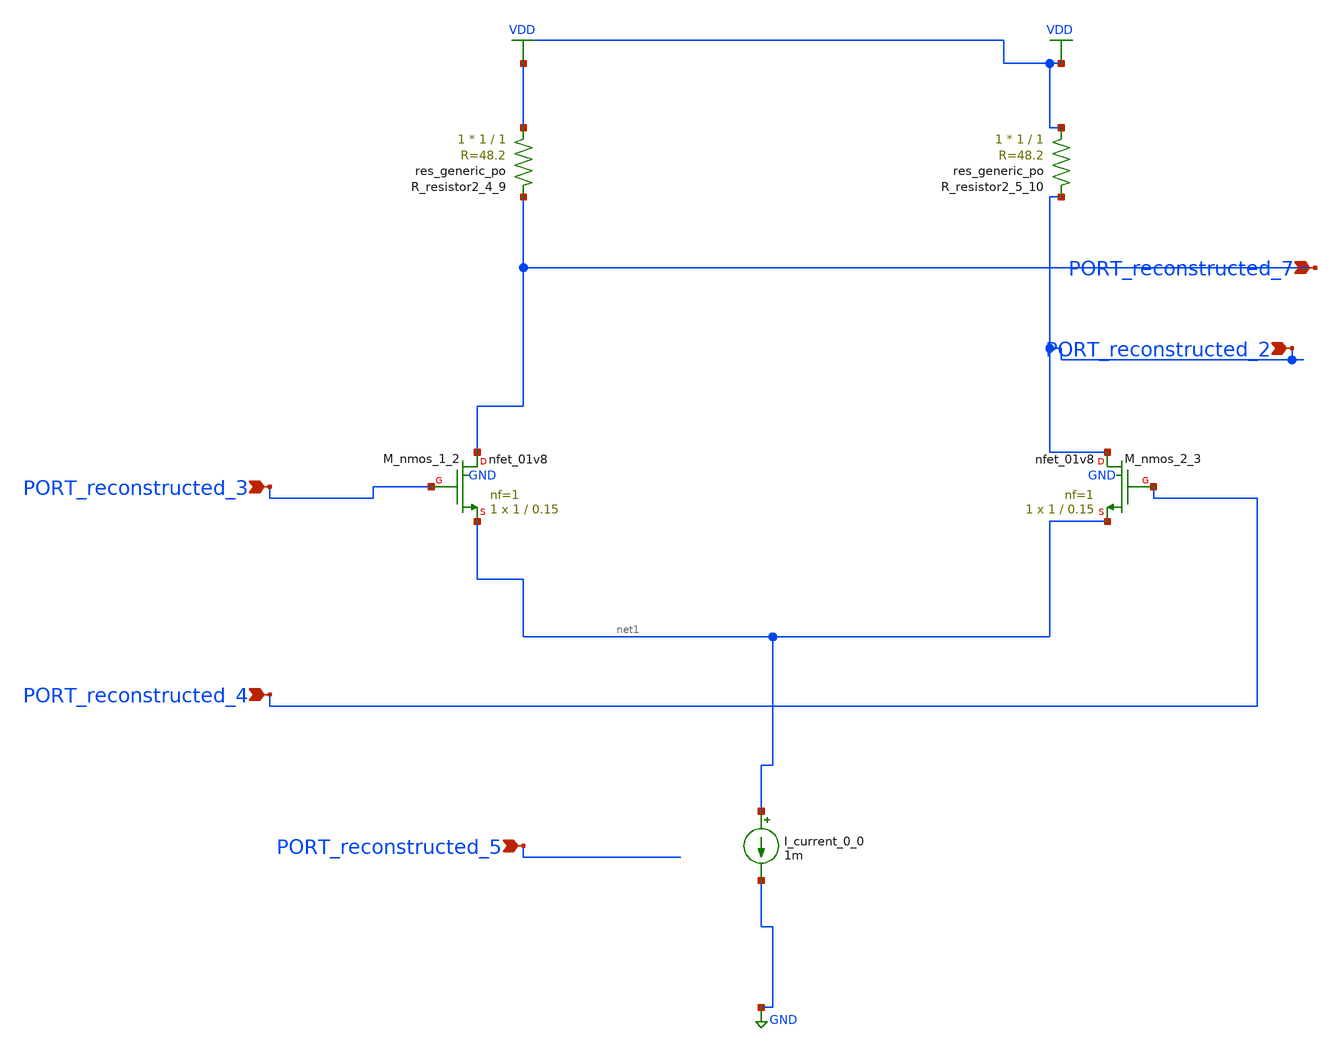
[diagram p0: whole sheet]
** sch_path: schematics/AMSNet/229.sch
**.subckt 229 PORT_reconstructed_7 PORT_reconstructed_2 PORT_reconstructed_3 PORT_reconstructed_4
*+ PORT_reconstructed_5
*.ipin PORT_reconstructed_7
*.ipin PORT_reconstructed_2
*.ipin PORT_reconstructed_3
*.ipin PORT_reconstructed_4
*.ipin PORT_reconstructed_5
I_current_0_0 net1 GND 1m
XM_nmos_1_2 PORT_reconstructed_7 PORT_reconstructed_3 net1 GND sky130_fd_pr__nfet_01v8 L=0.15 W=1 nf=1
+ ad='int((1 + 1)/2) * 1 / 1 * 0.29' as='int((1 + 2)/2) * 1 / 1 * 0.29' pd='2*int((1 + 1)/2) * (1 / 1 + 0.29)'
+ ps='2*int((1 + 2)/2) * (1 / 1 + 0.29)' nrd='0.29 / 1 ' nrs='0.29 / 1 ' sa=0 sb=0 sd=0 mult=1 m=1
XM_nmos_2_3 PORT_reconstructed_2 PORT_reconstructed_4 net1 GND sky130_fd_pr__nfet_01v8 L=0.15 W=1 nf=1
+ ad='int((1 + 1)/2) * 1 / 1 * 0.29' as='int((1 + 2)/2) * 1 / 1 * 0.29' pd='2*int((1 + 1)/2) * (1 / 1 + 0.29)'
+ ps='2*int((1 + 2)/2) * (1 / 1 + 0.29)' nrd='0.29 / 1 ' nrs='0.29 / 1 ' sa=0 sb=0 sd=0 mult=1 m=1
XR_resistor2_4_9 VDD PORT_reconstructed_7 sky130_fd_pr__res_generic_po W=1 L=1 m=1
XR_resistor2_5_10 VDD PORT_reconstructed_2 sky130_fd_pr__res_generic_po W=1 L=1 m=1
**.ends
.GLOBAL GND
.GLOBAL VDD
.end
